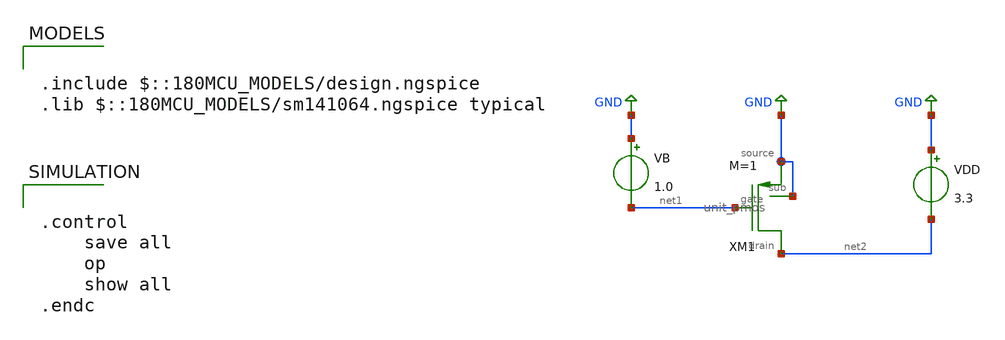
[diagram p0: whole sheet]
** sch_path: designs/libs/tb_single_mos/tb_single_pmos.sch
**.subckt tb_single_pmos
VB GND net1 1.0
VDD GND net2 3.3
XM1 net2 GND net1 GND unit_pmos M=1
**** begin user architecture code

.include $::180MCU_MODELS/design.ngspice
.lib $::180MCU_MODELS/sm141064.ngspice typical



.control
    save all
    op
    show all
.endc


**** end user architecture code
**.ends

* expanding   symbol:  libs/core_single_mos/unit_pmos/unit_pmos.sym # of pins=4
** sym_path: designs/libs/core_single_mos/unit_pmos/unit_pmos.sym
** sch_path: designs/libs/core_single_mos/unit_pmos/unit_pmos.sch
.subckt unit_pmos drain sub gate source
*.iopin drain
*.iopin source
*.iopin sub
*.iopin gate
**** begin user architecture code

.param M=1

**** end user architecture code
XM1 drain gate source sub pfet_03v3 L=0.5u W=48u nf=8 ad='int((nf+1)/2) * W/nf * 0.18u' as='int((nf+2)/2) * W/nf * 0.18u'
+ pd='2*int((nf+1)/2) * (W/nf + 0.18u)' ps='2*int((nf+2)/2) * (W/nf + 0.18u)' nrd='0.18u / W' nrs='0.18u / W'
+ sa=0 sb=0 sd=0 m={M}
.ends

.GLOBAL GND
.end
